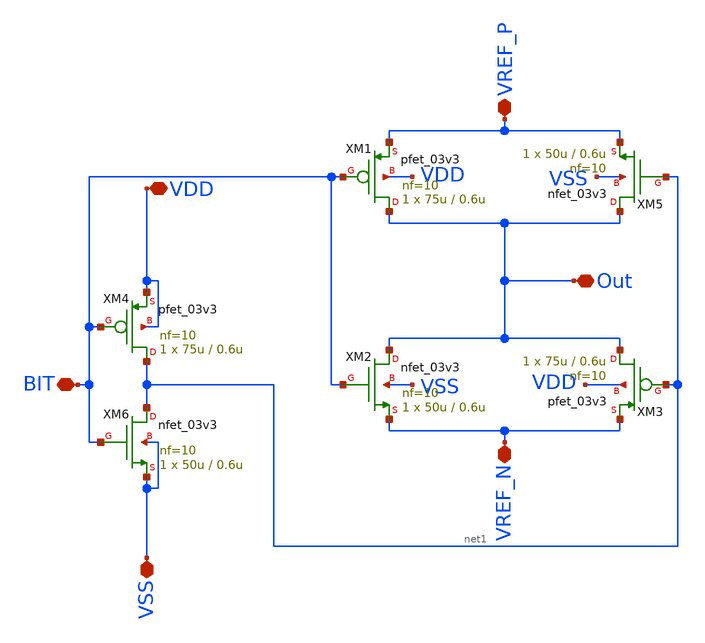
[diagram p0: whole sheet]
** sch_path: Schematics/DAC/TG_3v3.sch
**.subckt TG_3v3 VREF_P VREF_N Out BIT VDD VSS
*.iopin VREF_P
*.iopin VREF_N
*.iopin Out
*.iopin BIT
*.iopin VDD
*.iopin VSS
XM4 net1 BIT VDD VDD pfet_03v3 L=0.6u W=75u nf=10 ad='int((nf+1)/2) * W/nf * 0.18u' as='int((nf+2)/2) * W/nf * 0.18u'
+ pd='2*int((nf+1)/2) * (W/nf + 0.18u)' ps='2*int((nf+2)/2) * (W/nf + 0.18u)' nrd='0.18u / W' nrs='0.18u / W'
+ sa=0 sb=0 sd=0 m=1
XM6 net1 BIT VSS VSS nfet_03v3 L=0.6u W=50u nf=10 ad='int((nf+1)/2) * W/nf * 0.18u' as='int((nf+2)/2) * W/nf * 0.18u'
+ pd='2*int((nf+1)/2) * (W/nf + 0.18u)' ps='2*int((nf+2)/2) * (W/nf + 0.18u)' nrd='0.18u / W' nrs='0.18u / W'
+ sa=0 sb=0 sd=0 m=1
XM1 Out BIT VREF_P VDD pfet_03v3 L=0.6u W=75u nf=10 ad='int((nf+1)/2) * W/nf * 0.18u' as='int((nf+2)/2) * W/nf * 0.18u'
+ pd='2*int((nf+1)/2) * (W/nf + 0.18u)' ps='2*int((nf+2)/2) * (W/nf + 0.18u)' nrd='0.18u / W' nrs='0.18u / W'
+ sa=0 sb=0 sd=0 m=1
XM5 Out net1 VREF_P VSS nfet_03v3 L=0.6u W=50u nf=10 ad='int((nf+1)/2) * W/nf * 0.18u' as='int((nf+2)/2) * W/nf * 0.18u'
+ pd='2*int((nf+1)/2) * (W/nf + 0.18u)' ps='2*int((nf+2)/2) * (W/nf + 0.18u)' nrd='0.18u / W' nrs='0.18u / W'
+ sa=0 sb=0 sd=0 m=1
XM3 Out net1 VREF_N VDD pfet_03v3 L=0.6u W=75u nf=10 ad='int((nf+1)/2) * W/nf * 0.18u' as='int((nf+2)/2) * W/nf * 0.18u'
+ pd='2*int((nf+1)/2) * (W/nf + 0.18u)' ps='2*int((nf+2)/2) * (W/nf + 0.18u)' nrd='0.18u / W' nrs='0.18u / W'
+ sa=0 sb=0 sd=0 m=1
XM2 Out BIT VREF_N VSS nfet_03v3 L=0.6u W=50u nf=10 ad='int((nf+1)/2) * W/nf * 0.18u' as='int((nf+2)/2) * W/nf * 0.18u'
+ pd='2*int((nf+1)/2) * (W/nf + 0.18u)' ps='2*int((nf+2)/2) * (W/nf + 0.18u)' nrd='0.18u / W' nrs='0.18u / W'
+ sa=0 sb=0 sd=0 m=1
**.ends
.end
